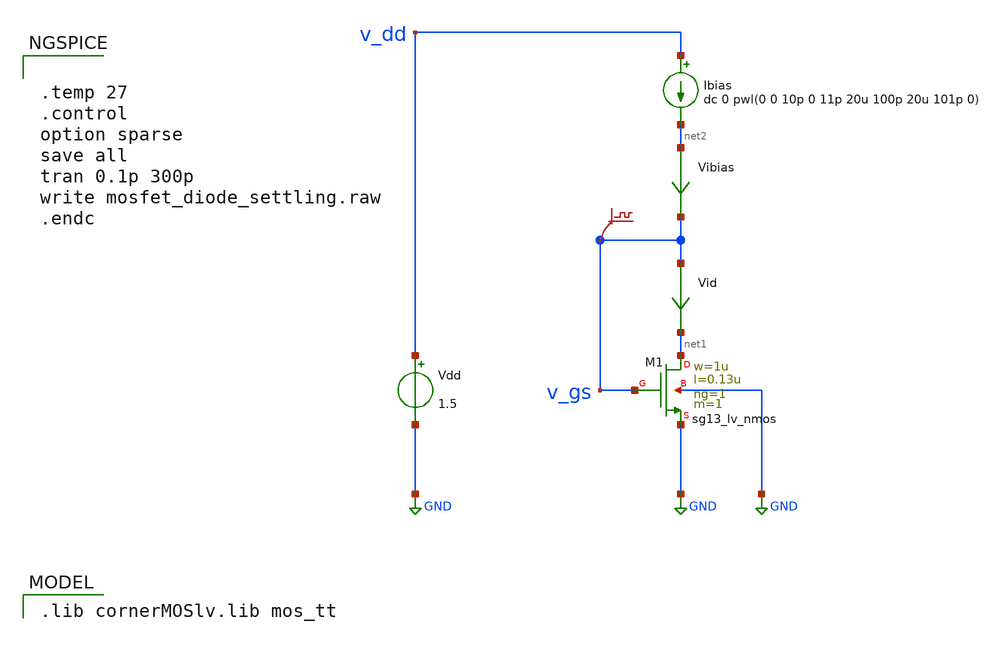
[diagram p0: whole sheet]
** sch_path: xschem/mosfet_diode_settling.sch
* (c) 2024 H. Pretl, Apache-2.0 license
**.subckt mosfet_diode_settling
Vdd v_dd GND 1.5
XM1 net1 v_gs GND GND sg13_lv_nmos w=1u l=0.13u ng=1 m=1 mm_ok=1
Ibias v_dd net2 dc 0 pwl(0 0 10p 0 11p 20u 100p 20u 101p 0)
.save v(v_gs)
Vid v_gs net1 0
.save i(vid)
Vibias net2 v_gs 0
.save i(vibias)
**** begin user architecture code
 .lib cornerMOSlv.lib mos_tt



.temp 27
.control
option sparse
save all
tran 0.1p 300p
write mosfet_diode_settling.raw
.endc


**** end user architecture code
**.ends
.GLOBAL GND
.end
